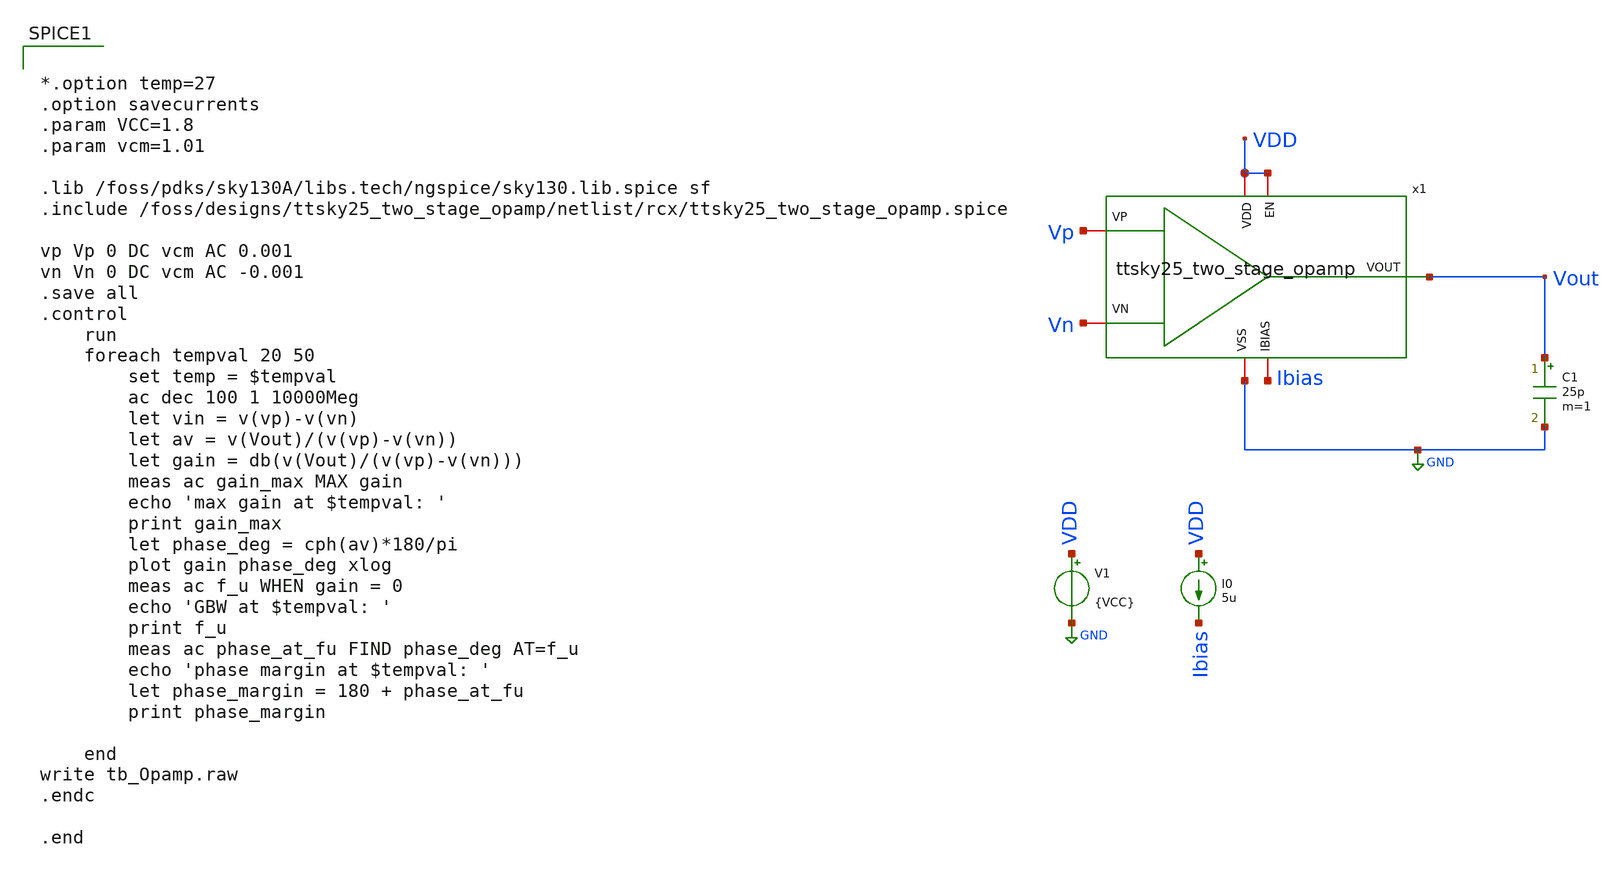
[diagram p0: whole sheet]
** sch_path: xschem/post-layout/testbenches/tb_Opamp.sch
**.subckt tb_Opamp
V1 VDD GND {VCC}
C1 Vout GND 25p m=1
I0 VDD Ibias 5u
x1 VDD Ibias Vout Vn Vp VDD GND ttsky25_two_stage_opamp
**** begin user architecture code


*.option temp=27
.option savecurrents
.param VCC=1.8
.param vcm=1.01

.lib /foss/pdks/sky130A/libs.tech/ngspice/sky130.lib.spice sf
.include /foss/designs/ttsky25_two_stage_opamp/netlist/rcx/ttsky25_two_stage_opamp.spice

vp Vp 0 DC vcm AC 0.001
vn Vn 0 DC vcm AC -0.001
.save all
.control
	run
	foreach tempval 20 50
		set temp = $tempval
		ac dec 100 1 10000Meg
		let vin = v(vp)-v(vn)
		let av = v(Vout)/(v(vp)-v(vn))
		let gain = db(v(Vout)/(v(vp)-v(vn)))
		meas ac gain_max MAX gain
		echo 'max gain at $tempval: '
		print gain_max
		let phase_deg = cph(av)*180/pi
		plot gain phase_deg xlog
		meas ac f_u WHEN gain = 0
		echo 'GBW at $tempval: '
		print f_u
		meas ac phase_at_fu FIND phase_deg AT=f_u
		echo 'phase margin at $tempval: '
		let phase_margin = 180 + phase_at_fu
		print phase_margin

	end
write tb_Opamp.raw
.endc

.end


**** end user architecture code
**.ends
.GLOBAL GND
.end
